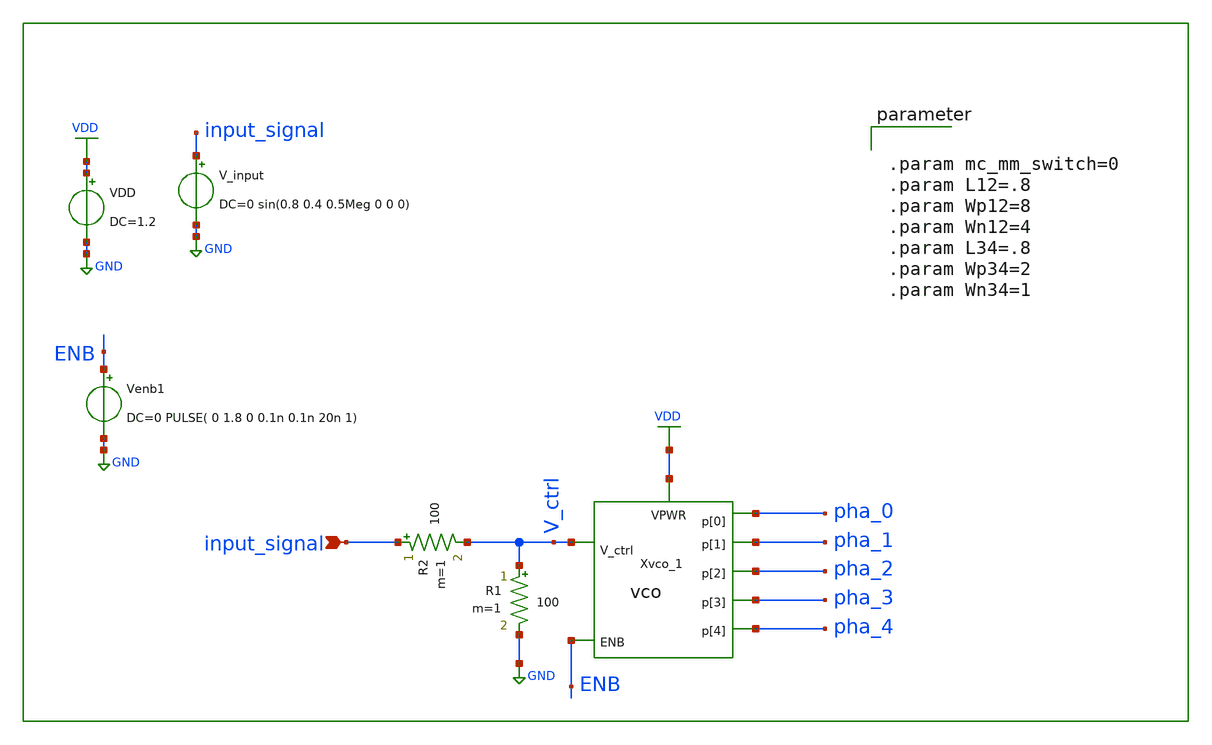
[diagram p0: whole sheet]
** sch_path: circuit_model/tb/vco_tb.sch
**.subckt vco_tb input_signal
*.ipin input_signal
Xvco_1 VDD pha_0 pha_1 pha_2 pha_3 pha_4 V_ctrl ENB vco L12="L12" Wp12="Wp12" Wn12="Wn12" L34="L34"
+ Wp34="Wp34" Wn34="Wn34"
VDD VDD GND DC=1.2
Venb1 ENB GND DC=0 PULSE( 0 1.8 0 0.1n 0.1n 20n 1)
V_input input_signal GND DC=0 sin(0.8 0.4 0.5Meg 0 0 0)
R1 V_ctrl GND 100 m=1
R2 input_signal V_ctrl 100 m=1
**** begin user architecture code


**LIB with Local Computer
.lib /home/toind/eda/uniccass/share/pdk/sky130A/libs.tech/ngspice/sky130.lib.spice tt
.inc /home/toind/eda/uniccass/share/pdk/sky130A/libs.ref/sky130_fd_sc_hd/spice/sky130_fd_sc_hd.spice




.control
*save all
set nobreak
set num_threads=5
set mode=1
if ($mode = 1)
    save all
    TRAN 1n 20u
    plot input_signal V_ctrl pha_0
    MEAS TRAN prd TRIG pha_0 VAL=0.8 RISE=2 TARG pha_0 VAL=0.8 RISE=8
    let freq=6/prd
    echo "Frequency: "
    print freq
end

if ($mode = 2)
    save "VDD" @Vsup[i] "p[0]"
    TRAN 1n 10u
    MEAS TRAN I_vco AVG @Vsup[i] FROM=2u TO=8u
    MEAS TRAN V_vco AVG VDD FROM=2u TO=8u
    let Power=I_vco*V_vco
    echo "Power: "
    print Power
end
.endc




.param mc_mm_switch=0
.param L12=.8
.param Wp12=8
.param Wn12=4
.param L34=.8
.param Wp34=2
.param Wn34=1


**** end user architecture code
**.ends

* expanding   symbol:  /home/toind/eda/ADC/circuit_model/lib/vco.sym # of pins=8
** sym_path: circuit_model/lib/vco.sym
** sch_path: circuit_model/lib/vco.sch
.subckt vco VPWR p[0] p[1] p[2] p[3] p[4] V_ctrl ENB  L12=0.15 Wp12=2.4 Wn12=1.2 L34=0.15 Wp34=1.2
+ Wn34=0.65
*.iopin VPWR
*.opin p[0]
*.ipin ENB
*.opin p[1]
*.opin p[2]
*.opin p[3]
*.opin p[4]
*.ipin V_ctrl
x1 VPWR ENB VGND VNB VPB VPWR pn[0] sky130_fd_sc_hd__einvp_1
Xro_1 V_ctrl VPWR p[0] p[1] p[2] p[3] p[4] pn[0] pn[1] pn[2] pn[3] pn[4] ring_osc L12="L12"
+ Wp12="Wp12" Wn12="Wn12" L34="L34" Wp34="Wp34" Wn34="Wn34"
.ends


* expanding   symbol:  ../lib/ring_osc.sym # of pins=12
** sym_path: circuit_model/lib/ring_osc.sym
** sch_path: circuit_model/lib/ring_osc.sch
.subckt ring_osc VGND VPWR p[0] p[1] p[2] p[3] p[4] pn[0] pn[1] pn[2] pn[3] pn[4]  L12=0.15 Wp12=2.4
+ Wn12=1.2 L34=0.15 Wp34=1.2 Wn34=0.65
*.iopin VPWR
*.iopin VGND
*.opin pn[0]
*.iopin p[0]
*.opin pn[1]
*.opin p[1]
*.opin p[2]
*.opin p[3]
*.opin p[4]
*.opin pn[2]
*.opin pn[3]
*.opin pn[4]
Xi_1 p[4] pn[4] VPWR VGND p[0] pn[0] cc_inv L12="L12" Wp12="Wp12" Wn12="Wn12" L34="L34" Wp34="Wp34"
+ Wn34="Wn34"
Xi_2 p[0] pn[0] VPWR VGND p[1] pn[1] cc_inv L12="L12" Wp12="Wp12" Wn12="Wn12" L34="L34" Wp34="Wp34"
+ Wn34="Wn34"
Xi_3 p[1] pn[1] VPWR VGND p[2] pn[2] cc_inv L12="L12" Wp12="Wp12" Wn12="Wn12" L34="L34" Wp34="Wp34"
+ Wn34="Wn34"
Xi_4 p[2] pn[2] VPWR VGND p[3] pn[3] cc_inv L12="L12" Wp12="Wp12" Wn12="Wn12" L34="L34" Wp34="Wp34"
+ Wn34="Wn34"
Xi_5 p[3] pn[3] VPWR VGND p[4] pn[4] cc_inv L12="L12" Wp12="Wp12" Wn12="Wn12" L34="L34" Wp34="Wp34"
+ Wn34="Wn34"
.ends


* expanding   symbol:  cc_inv.sym # of pins=6
** sym_path: circuit_model/lib/cc_inv.sym
** sch_path: circuit_model/lib/cc_inv.sch
.subckt cc_inv inp inn VPWR VGND outp outn  L12=0.15 Wp12=1.2 Wn12=0.65 L34=0.15 Wp34=1.2 Wn34=0.65
*.opin outp
*.ipin inn
*.iopin VGND
*.opin outn
*.ipin inp
*.iopin VPWR
Xi_1 inp VPWR VGND outp inverter L="L12" Wp="Wp12" Np=1 Wn="Wn12" Nn=1
Xi_3 outp VPWR VGND outn inverter L="L34" Wp="Wp34" Np=1 Wn="Wn34" Nn=1
Xi_2 inn VPWR VGND outn inverter L="L12" Wp="Wp12" Np=1 Wn="Wn12" Nn=1
Xi_4 outn VPWR VGND outp inverter L="L34" Wp="Wp34" Np=1 Wn="Wn34" Nn=1
.ends


* expanding   symbol:  inverter.sym # of pins=4
** sym_path: circuit_model/lib/inverter.sym
** sch_path: circuit_model/lib/inverter.sch
.subckt inverter A VPWR VGND Y  L=0.15 Wp=1.2 Np=1 Wn=0.65 Nn=1
*.iopin VPWR
*.iopin VGND
*.ipin A
*.opin Y
XM1 Y A VPWR VDD sky130_fd_pr__pfet_01v8 L="L" W="Wp" nf="Np" ad='int(("Np" + 1)/2) * "Wp" / "Np" * 0.29'
+ as='int(("Np" + 2)/2) * "Wp" / "Np" * 0.29' pd='2*int(("Np" + 1)/2) * ("Wp" / "Np" + 0.29)' ps='2*int(("Np" + 2)/2) * ("Wp" / "Np" + 0.29)'
+ nrd='0.29 / "Wp" ' nrs='0.29 / "Wp" ' sa=0 sb=0 sd=0 mult=1 m=1
XM2 Y A VGND GND sky130_fd_pr__nfet_01v8 L="L" W="Wn" nf="Nn" ad='int((nf+1)/2) * W/nf * 0.29' as='int((nf+2)/2) * W/nf * 0.29'
+ pd='2*int((nf+1)/2) * (W/nf + 0.29)' ps='2*int((nf+2)/2) * (W/nf + 0.29)' nrd='0.29 / W' nrs='0.29 / W'
+ sa=0 sb=0 sd=0 mult=1 m=1
.ends

.GLOBAL GND
.GLOBAL VDD
.end
